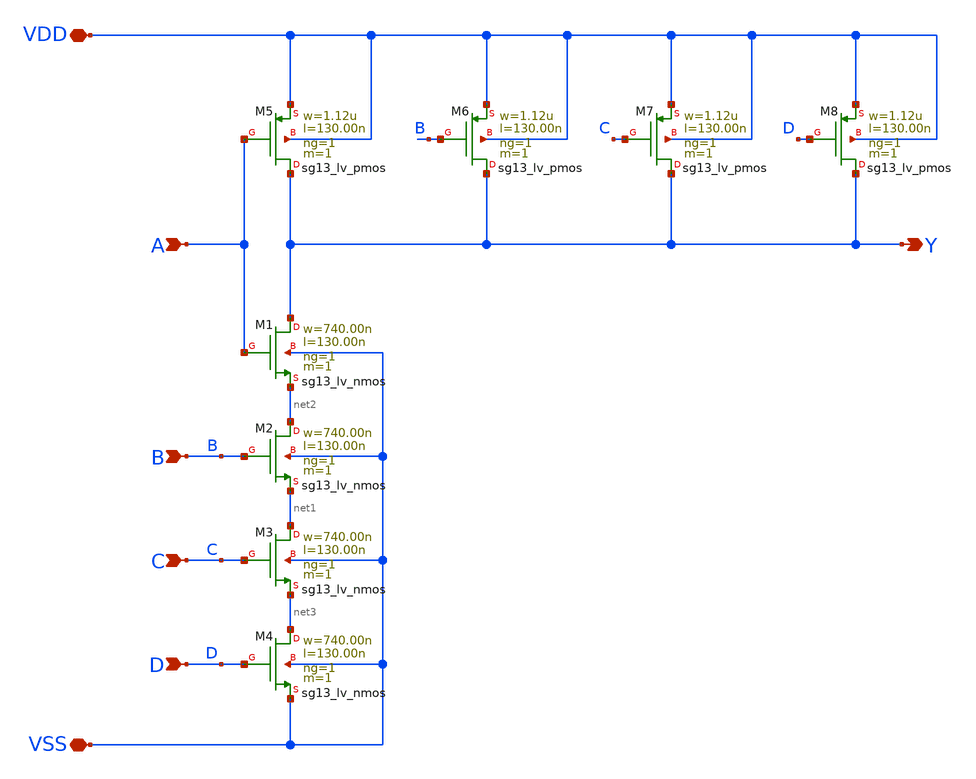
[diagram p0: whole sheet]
** sch_path: ihp-sg13g2/libs.tech/xschem/sg13g2_stdcells/sg13g2_nand4_1.sch
* Copyright 2023 IHP PDK Authors
* Licensed under the Apache License, Version 2.0 (the "License");
* you may not use this file except in compliance with the License.
* You may obtain a copy of the License at
* https://www.apache.org/licenses/LICENSE-2.0
* Unless required by applicable law or agreed to in writing, software
* distributed under the License is distributed on an "AS IS" BASIS,
* WITHOUT WARRANTIES OR CONDITIONS OF ANY KIND, either express or implied.
* See the License for the specific language governing permissions and
* limitations under the License.
**.subckt sg13g2_nand4_1 A B C Y D VDD VSS
*.ipin A
*.ipin B
*.ipin C
*.opin Y
*.ipin D
*.iopin VDD
*.iopin VSS
XM1 Y A net2 VSS sg13_lv_nmos w=740.00n l=130.00n ng=1 m=1 mm_ok=1
XM2 net2 B net1 VSS sg13_lv_nmos w=740.00n l=130.00n ng=1 m=1 mm_ok=1
XM3 net1 C net3 VSS sg13_lv_nmos w=740.00n l=130.00n ng=1 m=1 mm_ok=1
XM4 net3 D VSS VSS sg13_lv_nmos w=740.00n l=130.00n ng=1 m=1 mm_ok=1
XM5 Y A VDD VDD sg13_lv_pmos w=1.12u l=130.00n ng=1 m=1 mm_ok=1
XM6 Y B VDD VDD sg13_lv_pmos w=1.12u l=130.00n ng=1 m=1 mm_ok=1
XM7 Y C VDD VDD sg13_lv_pmos w=1.12u l=130.00n ng=1 m=1 mm_ok=1
XM8 Y D VDD VDD sg13_lv_pmos w=1.12u l=130.00n ng=1 m=1 mm_ok=1
**.ends
.end
